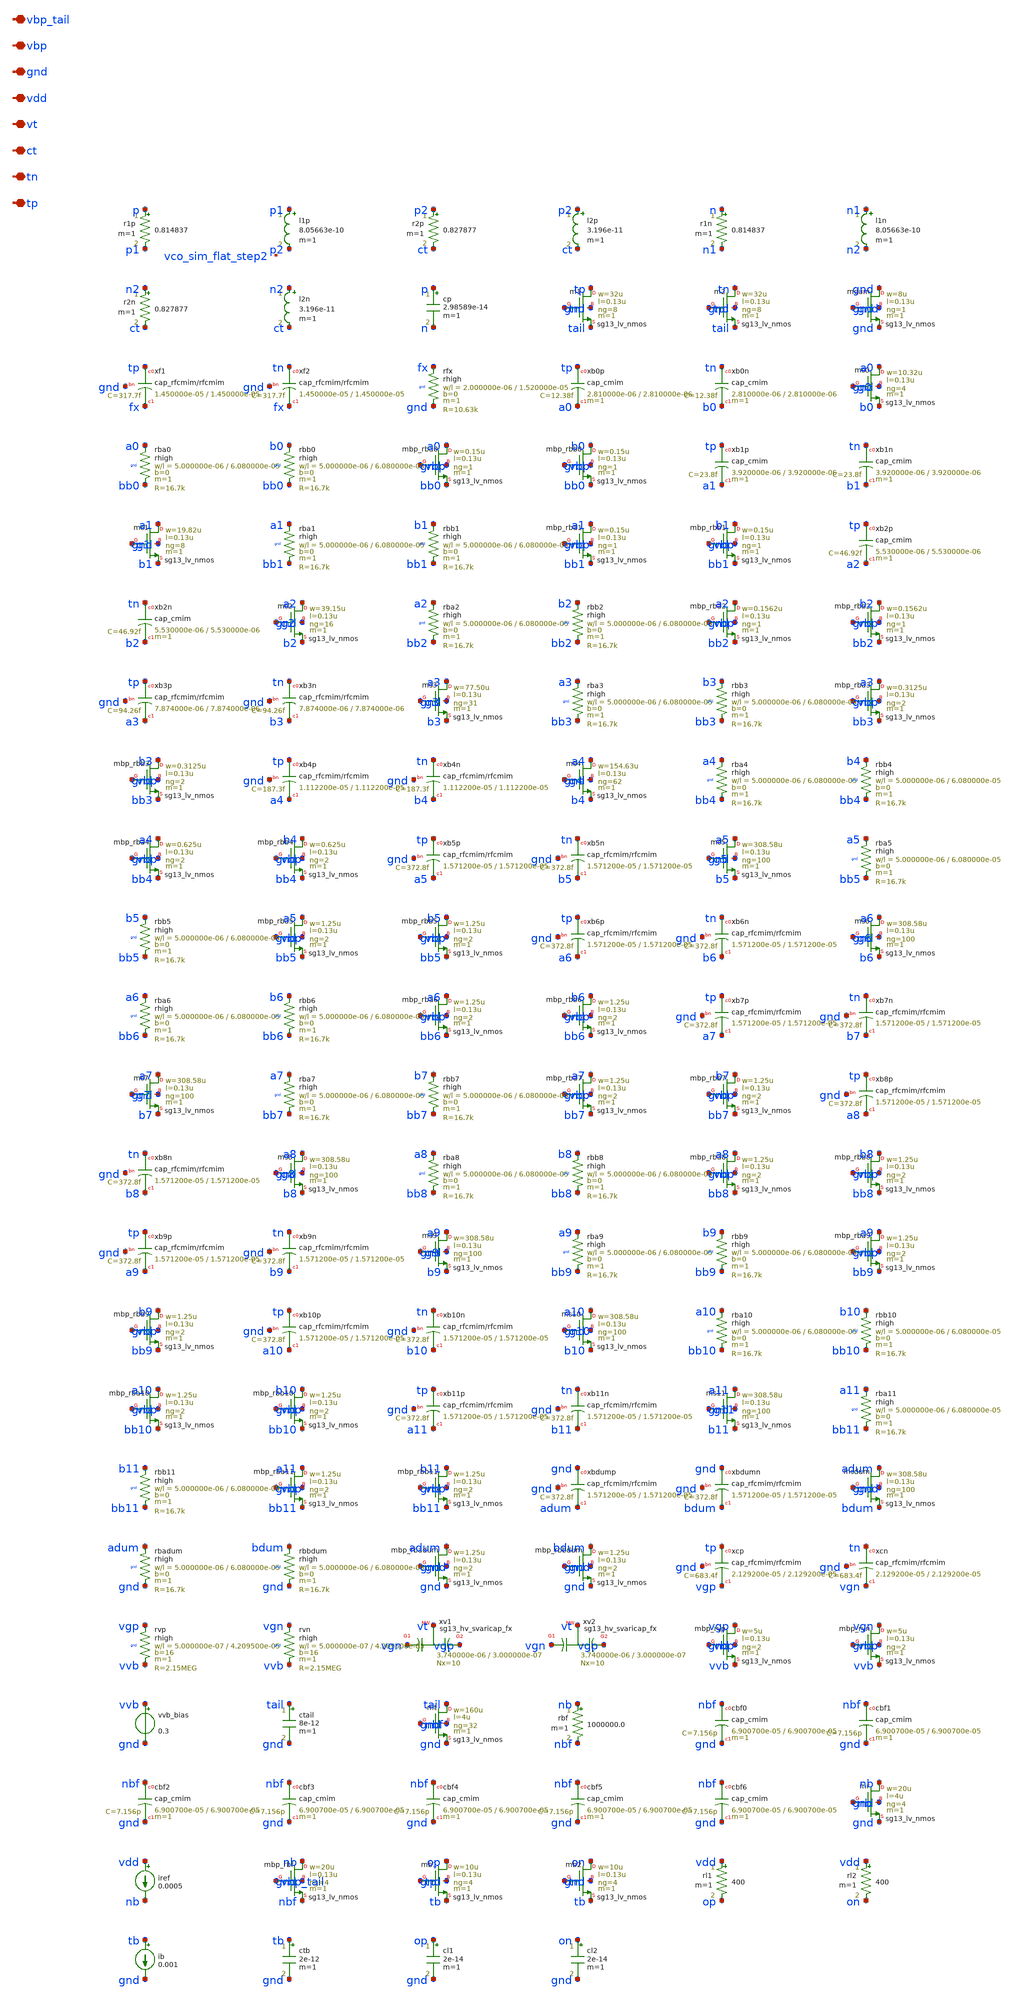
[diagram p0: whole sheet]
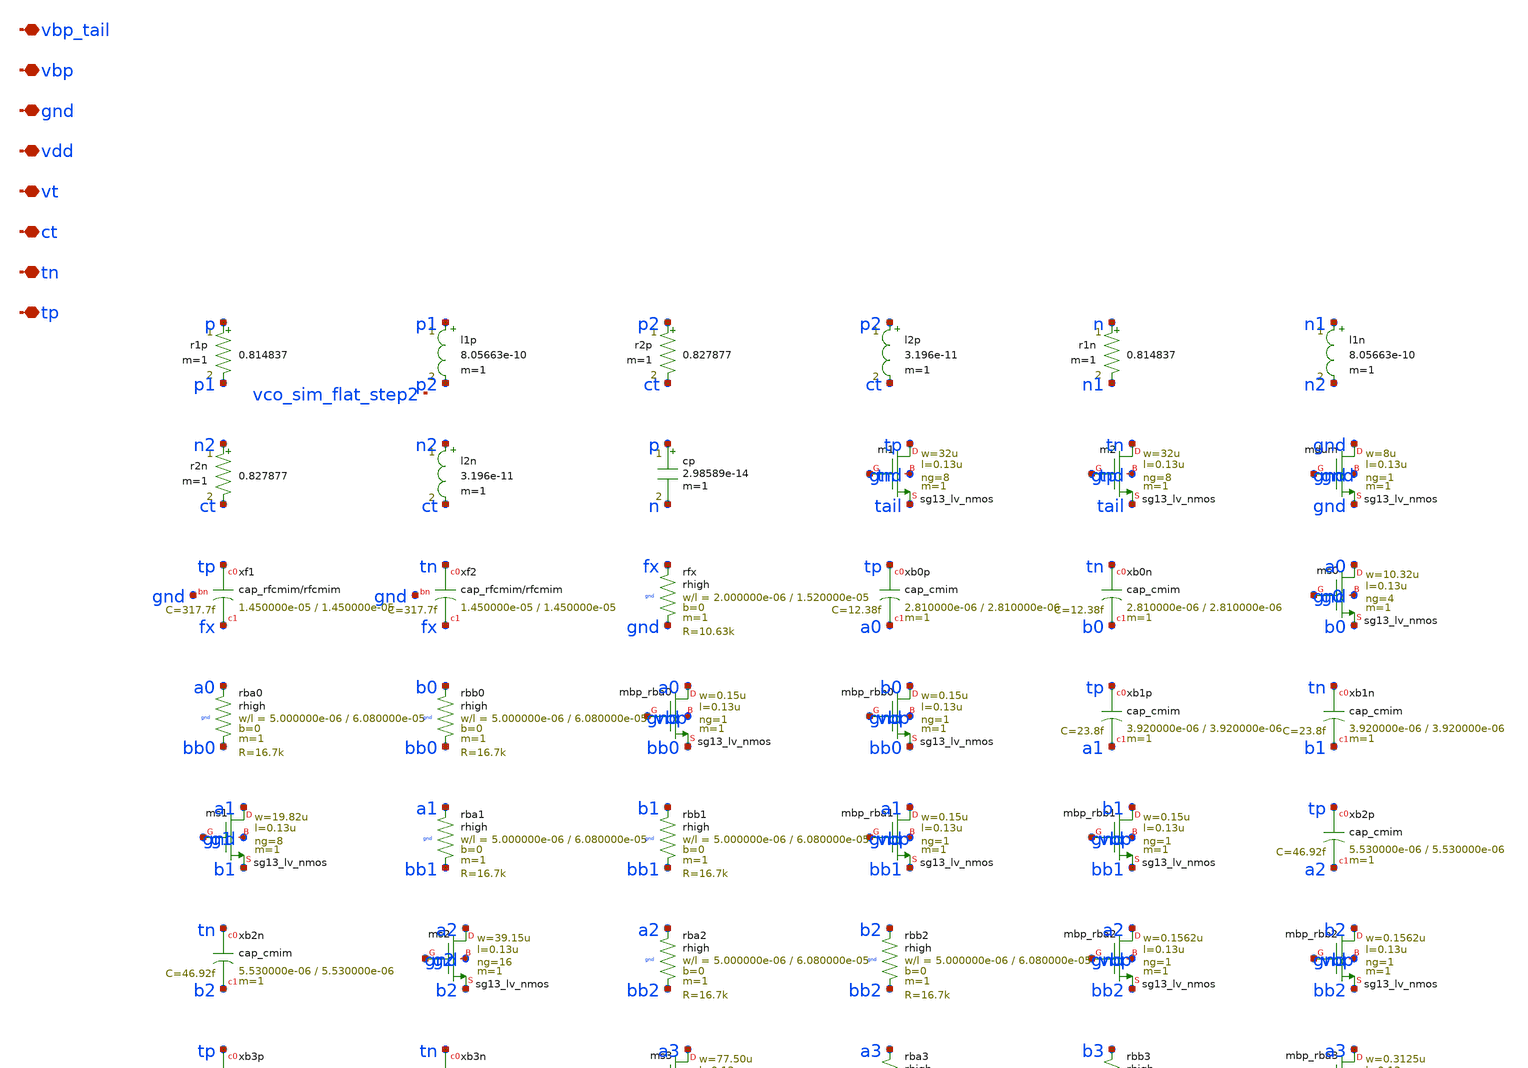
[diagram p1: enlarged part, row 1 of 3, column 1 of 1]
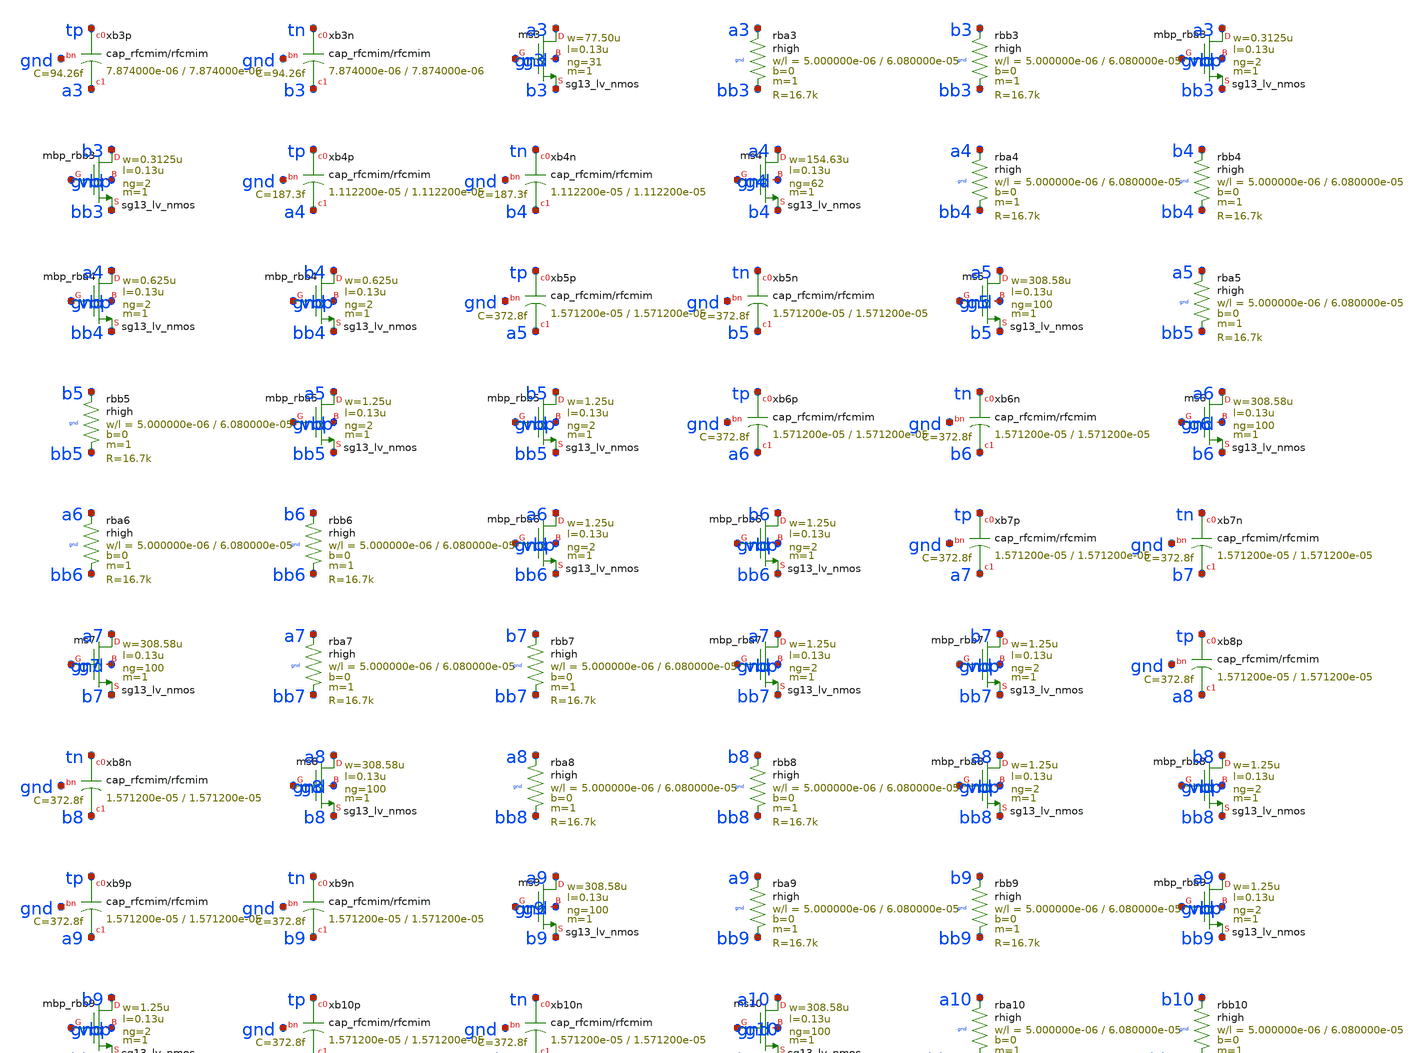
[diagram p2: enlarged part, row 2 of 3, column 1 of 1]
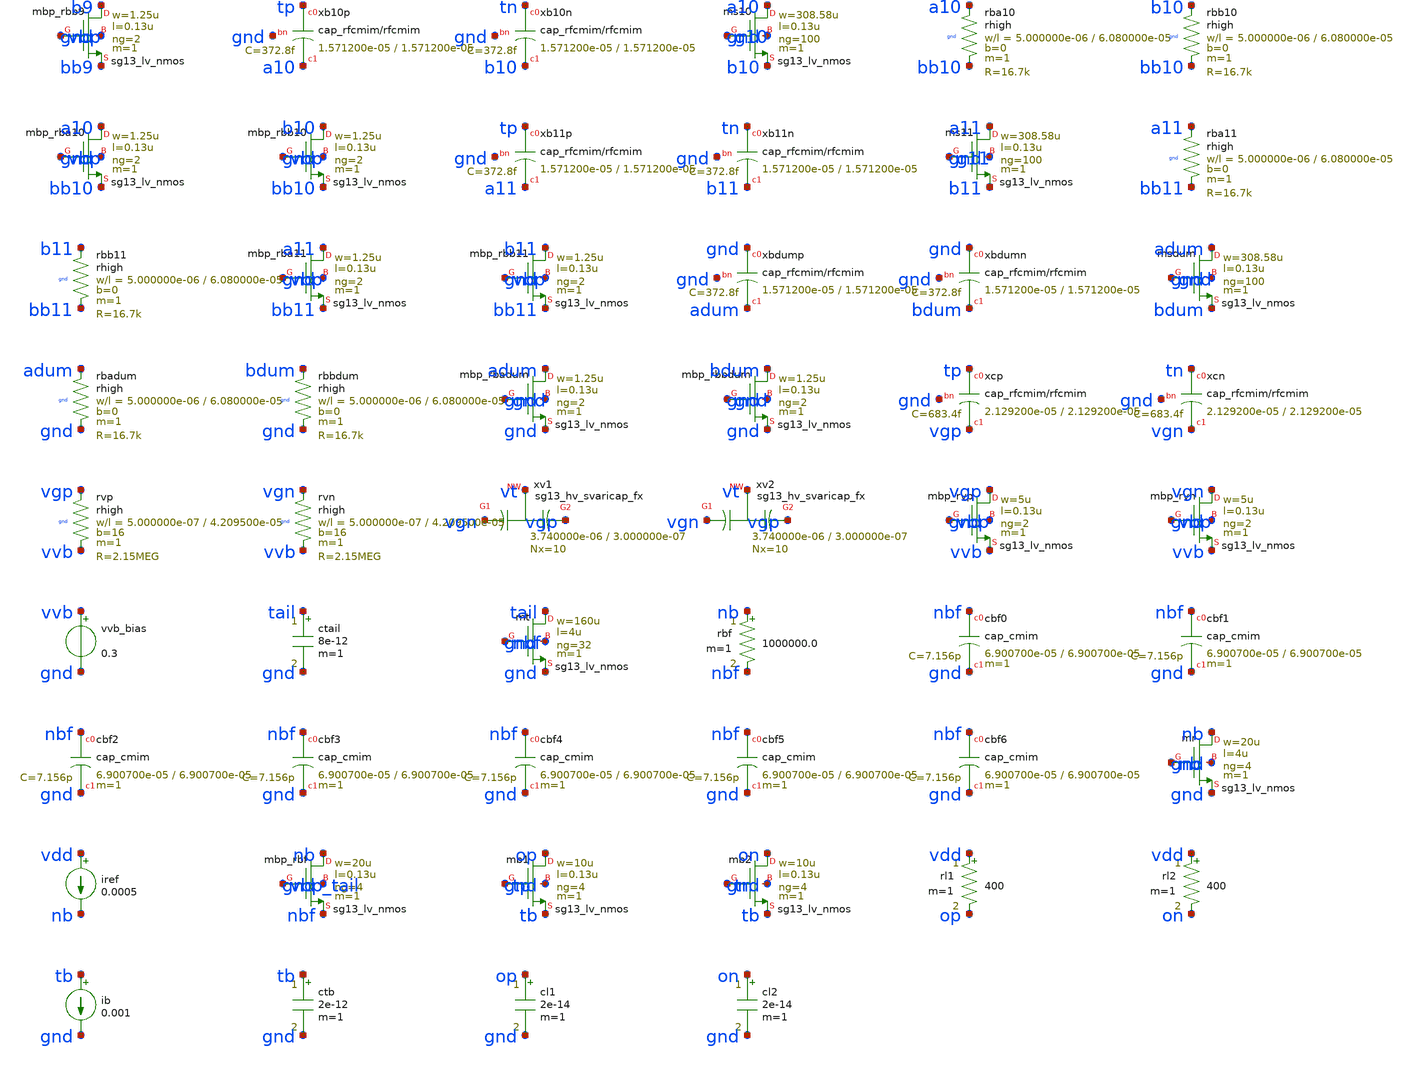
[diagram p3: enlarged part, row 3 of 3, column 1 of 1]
** sch_path: analog/vco/sch/vco_sim_flat.sch
**.subckt vco_sim_flat tp tn ct vt vdd gnd vbp vbp_tail
*.iopin tp
*.iopin tn
*.iopin ct
*.iopin vt
*.iopin vdd
*.iopin gnd
*.iopin vbp
*.iopin vbp_tail
r1p p p1 0.814837 m=1
l1p p1 p2 8.05663e-10 m=1
r2p p2 ct 0.827877 m=1
l2p p2 ct 3.196e-11 m=1
r1n n n1 0.814837 m=1
l1n n1 n2 8.05663e-10 m=1
r2n n2 ct 0.827877 m=1
l2n n2 ct 3.196e-11 m=1
cp p n 2.98589e-14 m=1
Xm1 tp tn tail gnd sg13_lv_nmos w=32u l=0.13u ng=8 m=1 mm_ok=1
Xm2 tn tp tail gnd sg13_lv_nmos w=32u l=0.13u ng=8 m=1 mm_ok=1
Xmdum gnd gnd gnd gnd sg13_lv_nmos w=8u l=0.13u ng=1 m=1 mm_ok=1
Xxf1 tp fx gnd cap_rfcmim w=1.450000e-05 l=1.450000e-05 wfeed=5.0e-6 m=1 mm_ok=1
Xxf2 tn fx gnd cap_rfcmim w=1.450000e-05 l=1.450000e-05 wfeed=5.0e-6 m=1 mm_ok=1
Xrfx fx gnd gnd rhigh w=2.000000e-06 l=1.520000e-05 m=1 b=0 mm_ok=1
Xxb0p tp a0 cap_cmim w=2.810000e-06 l=2.810000e-06 m=1 mm_ok=1
Xxb0n tn b0 cap_cmim w=2.810000e-06 l=2.810000e-06 m=1 mm_ok=1
Xms0 a0 g0 b0 gnd sg13_lv_nmos w=10.32u l=0.13u ng=4 m=1 mm_ok=1
Xrba0 a0 bb0 gnd rhigh w=5.000000e-06 l=6.080000e-05 m=1 b=0 mm_ok=1
Xrbb0 b0 bb0 gnd rhigh w=5.000000e-06 l=6.080000e-05 m=1 b=0 mm_ok=1
Xmbp_rba0 a0 vbp bb0 gnd sg13_lv_nmos w=0.15u l=0.13u ng=1 m=1 mm_ok=1
Xmbp_rbb0 b0 vbp bb0 gnd sg13_lv_nmos w=0.15u l=0.13u ng=1 m=1 mm_ok=1
Xxb1p tp a1 cap_cmim w=3.920000e-06 l=3.920000e-06 m=1 mm_ok=1
Xxb1n tn b1 cap_cmim w=3.920000e-06 l=3.920000e-06 m=1 mm_ok=1
Xms1 a1 g1 b1 gnd sg13_lv_nmos w=19.82u l=0.13u ng=8 m=1 mm_ok=1
Xrba1 a1 bb1 gnd rhigh w=5.000000e-06 l=6.080000e-05 m=1 b=0 mm_ok=1
Xrbb1 b1 bb1 gnd rhigh w=5.000000e-06 l=6.080000e-05 m=1 b=0 mm_ok=1
Xmbp_rba1 a1 vbp bb1 gnd sg13_lv_nmos w=0.15u l=0.13u ng=1 m=1 mm_ok=1
Xmbp_rbb1 b1 vbp bb1 gnd sg13_lv_nmos w=0.15u l=0.13u ng=1 m=1 mm_ok=1
Xxb2p tp a2 cap_cmim w=5.530000e-06 l=5.530000e-06 m=1 mm_ok=1
Xxb2n tn b2 cap_cmim w=5.530000e-06 l=5.530000e-06 m=1 mm_ok=1
Xms2 a2 g2 b2 gnd sg13_lv_nmos w=39.15u l=0.13u ng=16 m=1 mm_ok=1
Xrba2 a2 bb2 gnd rhigh w=5.000000e-06 l=6.080000e-05 m=1 b=0 mm_ok=1
Xrbb2 b2 bb2 gnd rhigh w=5.000000e-06 l=6.080000e-05 m=1 b=0 mm_ok=1
Xmbp_rba2 a2 vbp bb2 gnd sg13_lv_nmos w=0.1562u l=0.13u ng=1 m=1 mm_ok=1
Xmbp_rbb2 b2 vbp bb2 gnd sg13_lv_nmos w=0.1562u l=0.13u ng=1 m=1 mm_ok=1
Xxb3p tp a3 gnd cap_rfcmim w=7.874000e-06 l=7.874000e-06 wfeed=5.0e-6 m=1 mm_ok=1
Xxb3n tn b3 gnd cap_rfcmim w=7.874000e-06 l=7.874000e-06 wfeed=5.0e-6 m=1 mm_ok=1
Xms3 a3 g3 b3 gnd sg13_lv_nmos w=77.50u l=0.13u ng=31 m=1 mm_ok=1
Xrba3 a3 bb3 gnd rhigh w=5.000000e-06 l=6.080000e-05 m=1 b=0 mm_ok=1
Xrbb3 b3 bb3 gnd rhigh w=5.000000e-06 l=6.080000e-05 m=1 b=0 mm_ok=1
Xmbp_rba3 a3 vbp bb3 gnd sg13_lv_nmos w=0.3125u l=0.13u ng=2 m=1 mm_ok=1
Xmbp_rbb3 b3 vbp bb3 gnd sg13_lv_nmos w=0.3125u l=0.13u ng=2 m=1 mm_ok=1
Xxb4p tp a4 gnd cap_rfcmim w=1.112200e-05 l=1.112200e-05 wfeed=5.0e-6 m=1 mm_ok=1
Xxb4n tn b4 gnd cap_rfcmim w=1.112200e-05 l=1.112200e-05 wfeed=5.0e-6 m=1 mm_ok=1
Xms4 a4 g4 b4 gnd sg13_lv_nmos w=154.63u l=0.13u ng=62 m=1 mm_ok=1
Xrba4 a4 bb4 gnd rhigh w=5.000000e-06 l=6.080000e-05 m=1 b=0 mm_ok=1
Xrbb4 b4 bb4 gnd rhigh w=5.000000e-06 l=6.080000e-05 m=1 b=0 mm_ok=1
Xmbp_rba4 a4 vbp bb4 gnd sg13_lv_nmos w=0.625u l=0.13u ng=2 m=1 mm_ok=1
Xmbp_rbb4 b4 vbp bb4 gnd sg13_lv_nmos w=0.625u l=0.13u ng=2 m=1 mm_ok=1
Xxb5p tp a5 gnd cap_rfcmim w=1.571200e-05 l=1.571200e-05 wfeed=5.0e-6 m=1 mm_ok=1
Xxb5n tn b5 gnd cap_rfcmim w=1.571200e-05 l=1.571200e-05 wfeed=5.0e-6 m=1 mm_ok=1
Xms5 a5 g5 b5 gnd sg13_lv_nmos w=308.58u l=0.13u ng=100 m=1 mm_ok=1
Xrba5 a5 bb5 gnd rhigh w=5.000000e-06 l=6.080000e-05 m=1 b=0 mm_ok=1
Xrbb5 b5 bb5 gnd rhigh w=5.000000e-06 l=6.080000e-05 m=1 b=0 mm_ok=1
Xmbp_rba5 a5 vbp bb5 gnd sg13_lv_nmos w=1.25u l=0.13u ng=2 m=1 mm_ok=1
Xmbp_rbb5 b5 vbp bb5 gnd sg13_lv_nmos w=1.25u l=0.13u ng=2 m=1 mm_ok=1
Xxb6p tp a6 gnd cap_rfcmim w=1.571200e-05 l=1.571200e-05 wfeed=5.0e-6 m=1 mm_ok=1
Xxb6n tn b6 gnd cap_rfcmim w=1.571200e-05 l=1.571200e-05 wfeed=5.0e-6 m=1 mm_ok=1
Xms6 a6 g6 b6 gnd sg13_lv_nmos w=308.58u l=0.13u ng=100 m=1 mm_ok=1
Xrba6 a6 bb6 gnd rhigh w=5.000000e-06 l=6.080000e-05 m=1 b=0 mm_ok=1
Xrbb6 b6 bb6 gnd rhigh w=5.000000e-06 l=6.080000e-05 m=1 b=0 mm_ok=1
Xmbp_rba6 a6 vbp bb6 gnd sg13_lv_nmos w=1.25u l=0.13u ng=2 m=1 mm_ok=1
Xmbp_rbb6 b6 vbp bb6 gnd sg13_lv_nmos w=1.25u l=0.13u ng=2 m=1 mm_ok=1
Xxb7p tp a7 gnd cap_rfcmim w=1.571200e-05 l=1.571200e-05 wfeed=5.0e-6 m=1 mm_ok=1
Xxb7n tn b7 gnd cap_rfcmim w=1.571200e-05 l=1.571200e-05 wfeed=5.0e-6 m=1 mm_ok=1
Xms7 a7 g7 b7 gnd sg13_lv_nmos w=308.58u l=0.13u ng=100 m=1 mm_ok=1
Xrba7 a7 bb7 gnd rhigh w=5.000000e-06 l=6.080000e-05 m=1 b=0 mm_ok=1
Xrbb7 b7 bb7 gnd rhigh w=5.000000e-06 l=6.080000e-05 m=1 b=0 mm_ok=1
Xmbp_rba7 a7 vbp bb7 gnd sg13_lv_nmos w=1.25u l=0.13u ng=2 m=1 mm_ok=1
Xmbp_rbb7 b7 vbp bb7 gnd sg13_lv_nmos w=1.25u l=0.13u ng=2 m=1 mm_ok=1
Xxb8p tp a8 gnd cap_rfcmim w=1.571200e-05 l=1.571200e-05 wfeed=5.0e-6 m=1 mm_ok=1
Xxb8n tn b8 gnd cap_rfcmim w=1.571200e-05 l=1.571200e-05 wfeed=5.0e-6 m=1 mm_ok=1
Xms8 a8 g8 b8 gnd sg13_lv_nmos w=308.58u l=0.13u ng=100 m=1 mm_ok=1
Xrba8 a8 bb8 gnd rhigh w=5.000000e-06 l=6.080000e-05 m=1 b=0 mm_ok=1
Xrbb8 b8 bb8 gnd rhigh w=5.000000e-06 l=6.080000e-05 m=1 b=0 mm_ok=1
Xmbp_rba8 a8 vbp bb8 gnd sg13_lv_nmos w=1.25u l=0.13u ng=2 m=1 mm_ok=1
Xmbp_rbb8 b8 vbp bb8 gnd sg13_lv_nmos w=1.25u l=0.13u ng=2 m=1 mm_ok=1
Xxb9p tp a9 gnd cap_rfcmim w=1.571200e-05 l=1.571200e-05 wfeed=5.0e-6 m=1 mm_ok=1
Xxb9n tn b9 gnd cap_rfcmim w=1.571200e-05 l=1.571200e-05 wfeed=5.0e-6 m=1 mm_ok=1
Xms9 a9 g9 b9 gnd sg13_lv_nmos w=308.58u l=0.13u ng=100 m=1 mm_ok=1
Xrba9 a9 bb9 gnd rhigh w=5.000000e-06 l=6.080000e-05 m=1 b=0 mm_ok=1
Xrbb9 b9 bb9 gnd rhigh w=5.000000e-06 l=6.080000e-05 m=1 b=0 mm_ok=1
Xmbp_rba9 a9 vbp bb9 gnd sg13_lv_nmos w=1.25u l=0.13u ng=2 m=1 mm_ok=1
Xmbp_rbb9 b9 vbp bb9 gnd sg13_lv_nmos w=1.25u l=0.13u ng=2 m=1 mm_ok=1
Xxb10p tp a10 gnd cap_rfcmim w=1.571200e-05 l=1.571200e-05 wfeed=5.0e-6 m=1 mm_ok=1
Xxb10n tn b10 gnd cap_rfcmim w=1.571200e-05 l=1.571200e-05 wfeed=5.0e-6 m=1 mm_ok=1
Xms10 a10 g10 b10 gnd sg13_lv_nmos w=308.58u l=0.13u ng=100 m=1 mm_ok=1
Xrba10 a10 bb10 gnd rhigh w=5.000000e-06 l=6.080000e-05 m=1 b=0 mm_ok=1
Xrbb10 b10 bb10 gnd rhigh w=5.000000e-06 l=6.080000e-05 m=1 b=0 mm_ok=1
Xmbp_rba10 a10 vbp bb10 gnd sg13_lv_nmos w=1.25u l=0.13u ng=2 m=1 mm_ok=1
Xmbp_rbb10 b10 vbp bb10 gnd sg13_lv_nmos w=1.25u l=0.13u ng=2 m=1 mm_ok=1
Xxb11p tp a11 gnd cap_rfcmim w=1.571200e-05 l=1.571200e-05 wfeed=5.0e-6 m=1 mm_ok=1
Xxb11n tn b11 gnd cap_rfcmim w=1.571200e-05 l=1.571200e-05 wfeed=5.0e-6 m=1 mm_ok=1
Xms11 a11 g11 b11 gnd sg13_lv_nmos w=308.58u l=0.13u ng=100 m=1 mm_ok=1
Xrba11 a11 bb11 gnd rhigh w=5.000000e-06 l=6.080000e-05 m=1 b=0 mm_ok=1
Xrbb11 b11 bb11 gnd rhigh w=5.000000e-06 l=6.080000e-05 m=1 b=0 mm_ok=1
Xmbp_rba11 a11 vbp bb11 gnd sg13_lv_nmos w=1.25u l=0.13u ng=2 m=1 mm_ok=1
Xmbp_rbb11 b11 vbp bb11 gnd sg13_lv_nmos w=1.25u l=0.13u ng=2 m=1 mm_ok=1
Xxbdump gnd adum gnd cap_rfcmim w=1.571200e-05 l=1.571200e-05 wfeed=5.0e-6 m=1 mm_ok=1
Xxbdumn gnd bdum gnd cap_rfcmim w=1.571200e-05 l=1.571200e-05 wfeed=5.0e-6 m=1 mm_ok=1
Xmsdum adum gnd bdum gnd sg13_lv_nmos w=308.58u l=0.13u ng=100 m=1 mm_ok=1
Xrbadum adum gnd gnd rhigh w=5.000000e-06 l=6.080000e-05 m=1 b=0 mm_ok=1
Xrbbdum bdum gnd gnd rhigh w=5.000000e-06 l=6.080000e-05 m=1 b=0 mm_ok=1
Xmbp_rbadum adum gnd gnd gnd sg13_lv_nmos w=1.25u l=0.13u ng=2 m=1 mm_ok=1
Xmbp_rbbdum bdum gnd gnd gnd sg13_lv_nmos w=1.25u l=0.13u ng=2 m=1 mm_ok=1
Xxcp tp vgp gnd cap_rfcmim w=2.129200e-05 l=2.129200e-05 wfeed=5.0e-6 m=1 mm_ok=1
Xxcn tn vgn gnd cap_rfcmim w=2.129200e-05 l=2.129200e-05 wfeed=5.0e-6 m=1 mm_ok=1
Xrvp vgp vvb gnd rhigh w=5.000000e-07 l=4.209500e-05 m=1 b=16 mm_ok=1
Xrvn vgn vvb gnd rhigh w=5.000000e-07 l=4.209500e-05 m=1 b=16 mm_ok=1
Xxv1 vgn vt vgp sub! sg13_hv_svaricap_fx w=3.740000e-06 l=3.000000e-07 Nx=10 mm_ok=1
Xxv2 vgn vt vgp sub! sg13_hv_svaricap_fx w=3.740000e-06 l=3.000000e-07 Nx=10 mm_ok=1
Xmbp_rvp vgp vbp vvb gnd sg13_lv_nmos w=5u l=0.13u ng=2 m=1 mm_ok=1
Xmbp_rvn vgn vbp vvb gnd sg13_lv_nmos w=5u l=0.13u ng=2 m=1 mm_ok=1
vvb_bias vvb gnd 0.3
ctail tail gnd 8e-12 m=1
Xmt tail nbf gnd gnd sg13_lv_nmos w=160u l=4u ng=32 m=1 mm_ok=1
rbf nb nbf 1000000.0 m=1
Xcbf0 nbf gnd cap_cmim w=6.900700e-05 l=6.900700e-05 m=1 mm_ok=1
Xcbf1 nbf gnd cap_cmim w=6.900700e-05 l=6.900700e-05 m=1 mm_ok=1
Xcbf2 nbf gnd cap_cmim w=6.900700e-05 l=6.900700e-05 m=1 mm_ok=1
Xcbf3 nbf gnd cap_cmim w=6.900700e-05 l=6.900700e-05 m=1 mm_ok=1
Xcbf4 nbf gnd cap_cmim w=6.900700e-05 l=6.900700e-05 m=1 mm_ok=1
Xcbf5 nbf gnd cap_cmim w=6.900700e-05 l=6.900700e-05 m=1 mm_ok=1
Xcbf6 nbf gnd cap_cmim w=6.900700e-05 l=6.900700e-05 m=1 mm_ok=1
Xmr nb nb gnd gnd sg13_lv_nmos w=20u l=4u ng=4 m=1 mm_ok=1
iref vdd nb 0.0005
Xmbp_rbf nb vbp_tail nbf gnd sg13_lv_nmos w=20u l=0.13u ng=4 m=1 mm_ok=1
Xmb1 op tp tb gnd sg13_lv_nmos w=10u l=0.13u ng=4 m=1 mm_ok=1
Xmb2 on tn tb gnd sg13_lv_nmos w=10u l=0.13u ng=4 m=1 mm_ok=1
rl1 vdd op 400 m=1
rl2 vdd on 400 m=1
ib tb gnd 0.001
ctb tb gnd 2e-12 m=1
cl1 op gnd 2e-14 m=1
cl2 on gnd 2e-14 m=1
**.ends
.end
